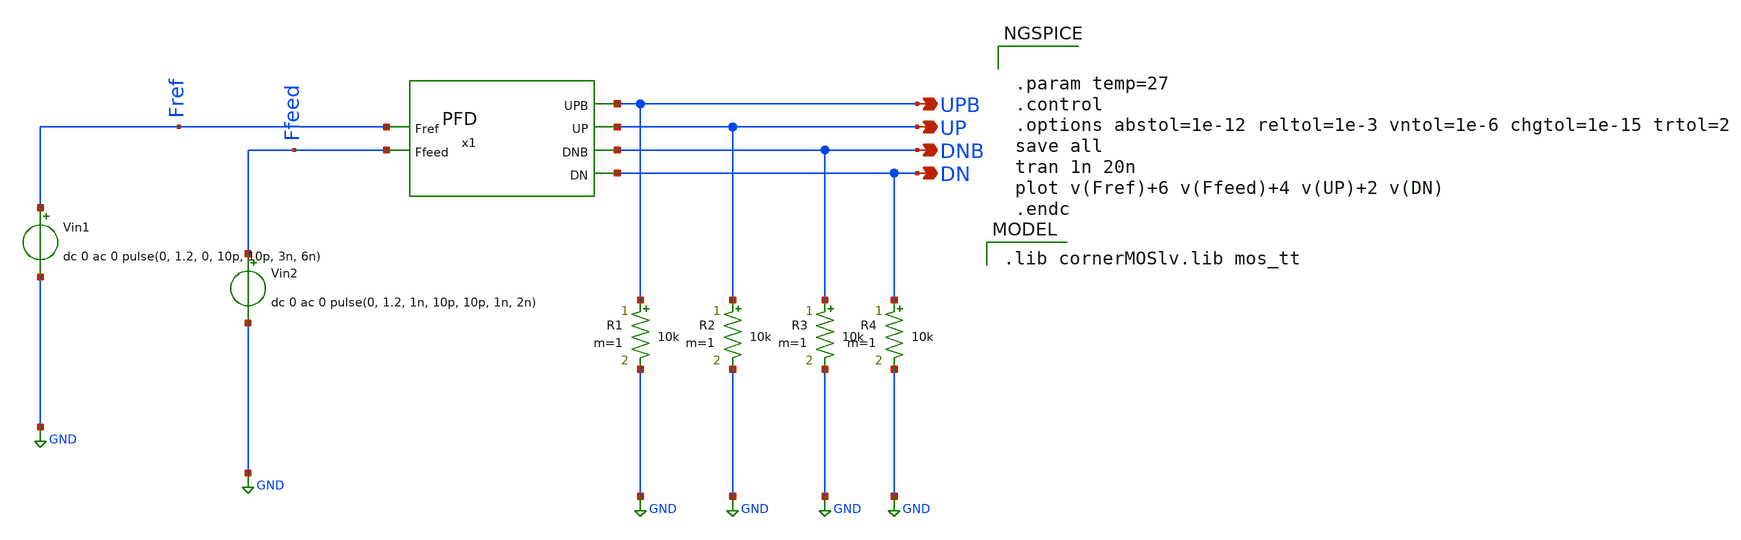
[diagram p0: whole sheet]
** sch_path: Team Designs/Team 1 Design/design_data/xschem/PFD/PFD_tb.sch
**.subckt PFD_tb UPB UP DNB DN
*.opin UPB
*.opin UP
*.opin DNB
*.opin DN
Vin1 Fref GND dc 0 ac 0 pulse(0, 1.2, 0, 10p, 10p, 3n, 6n)
Vin2 Ffeed GND dc 0 ac 0 pulse(0, 1.2, 1n, 10p, 10p, 1n, 2n)
R1 UPB GND 10k m=1
R2 UP GND 10k m=1
R3 DNB GND 10k m=1
R4 DN GND 10k m=1
x1 Fref UP UPB DN DNB Ffeed PFD
**** begin user architecture code
 .lib cornerMOSlv.lib mos_tt



.param temp=27
.control
.options abstol=1e-12 reltol=1e-3 vntol=1e-6 chgtol=1e-15 trtol=2
save all
tran 1n 20n
plot v(Fref)+6 v(Ffeed)+4 v(UP)+2 v(DN)
.endc


**** end user architecture code
**.ends
.GLOBAL GND
.end
